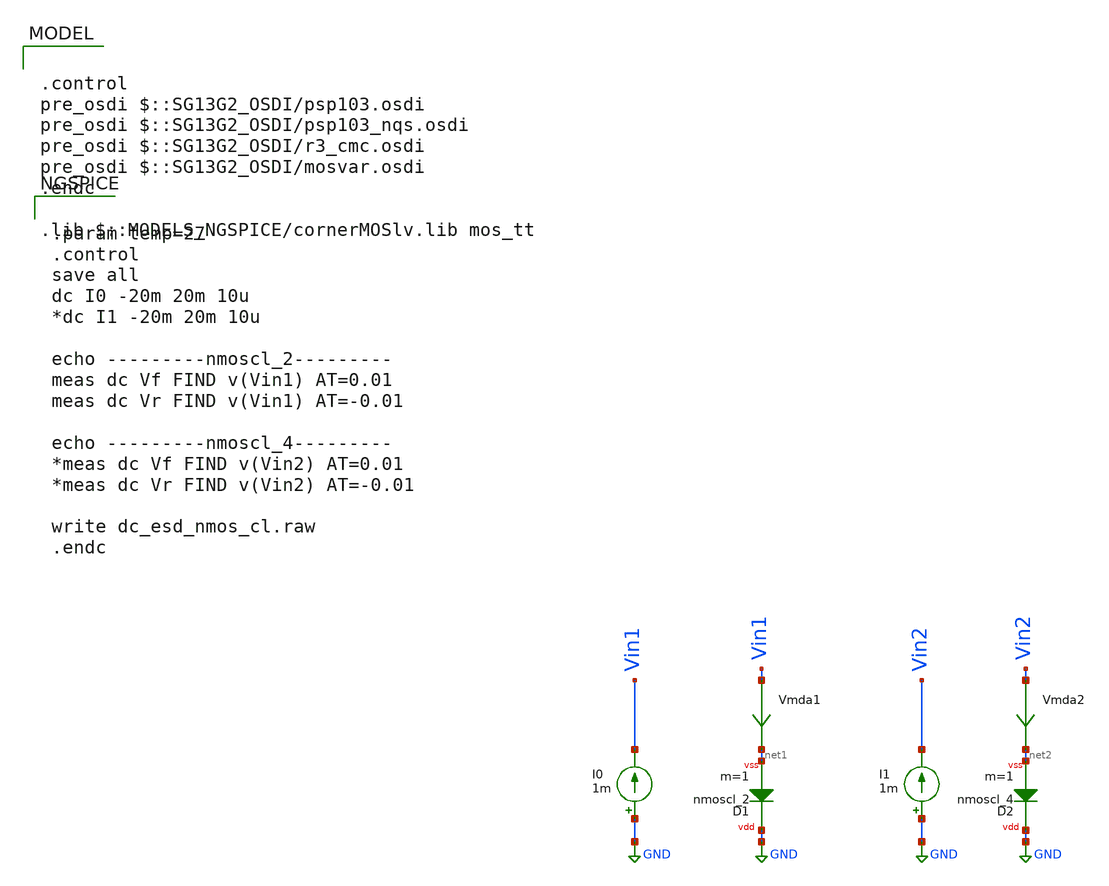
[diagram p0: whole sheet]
** sch_path: ihp-sg13g2/xschem_libs/sg13g2_tests/dc_esd_nmos_cl/schematic/dc_esd_nmos_cl.sch
**.subckt dc_esd_nmos_cl
Vmda1 Vin1 net1 0
.save i(vmda1)
I0 GND Vin1 1m
Vmda2 Vin2 net2 0
.save i(vmda2)
I1 GND Vin2 1m
XD1 GND net1 nmoscl_2 m=1
XD2 GND net2 nmoscl_4 m=1
**** begin user architecture code

.control
pre_osdi $::SG13G2_OSDI/psp103.osdi
pre_osdi $::SG13G2_OSDI/psp103_nqs.osdi
pre_osdi $::SG13G2_OSDI/r3_cmc.osdi
pre_osdi $::SG13G2_OSDI/mosvar.osdi
.endc

.lib $::MODELS_NGSPICE/cornerMOSlv.lib mos_tt



.param temp=27
.control
save all
dc I0 -20m 20m 10u
*dc I1 -20m 20m 10u

echo ---------nmoscl_2---------
meas dc Vf FIND v(Vin1) AT=0.01
meas dc Vr FIND v(Vin1) AT=-0.01

echo ---------nmoscl_4---------
*meas dc Vf FIND v(Vin2) AT=0.01
*meas dc Vr FIND v(Vin2) AT=-0.01

write dc_esd_nmos_cl.raw
.endc


**** end user architecture code
**.ends
.GLOBAL GND
.end
